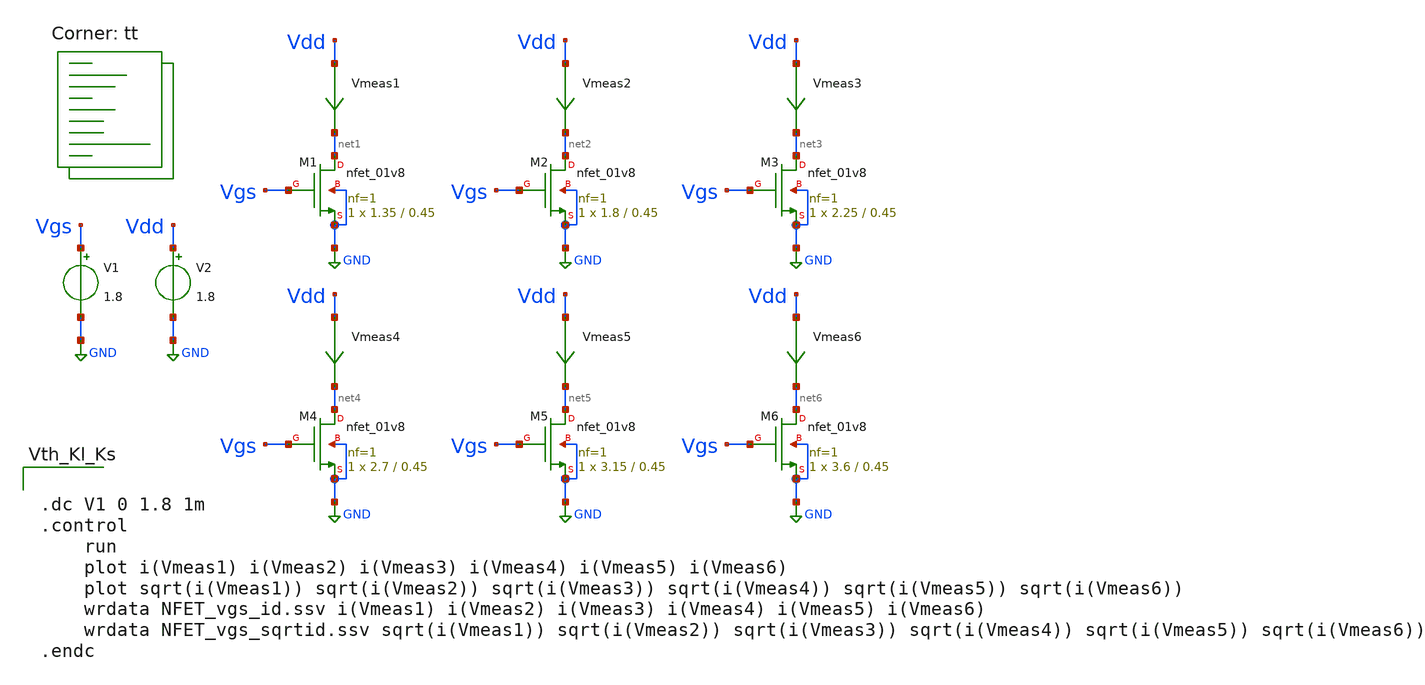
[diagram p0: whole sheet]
** sch_path: opamp_design/Parametros_cmos/NFET_param1.sch
**.subckt NFET_param1
XM1 net1 Vgs GND GND sky130_fd_pr__nfet_01v8 L=0.45 W=1.35 nf=1 ad='int((nf+1)/2) * W/nf * 0.29' as='int((nf+2)/2) * W/nf * 0.29'
+ pd='2*int((nf+1)/2) * (W/nf + 0.29)' ps='2*int((nf+2)/2) * (W/nf + 0.29)' nrd='0.29 / W' nrs='0.29 / W'
+ sa=0 sb=0 sd=0 mult=1 m=1
Vmeas1 Vdd net1 0
.save i(vmeas1)
V2 Vdd GND 1.8
V1 Vgs GND 1.8
XM2 net2 Vgs GND GND sky130_fd_pr__nfet_01v8 L=0.45 W=1.8 nf=1 ad='int((nf+1)/2) * W/nf * 0.29' as='int((nf+2)/2) * W/nf * 0.29'
+ pd='2*int((nf+1)/2) * (W/nf + 0.29)' ps='2*int((nf+2)/2) * (W/nf + 0.29)' nrd='0.29 / W' nrs='0.29 / W'
+ sa=0 sb=0 sd=0 mult=1 m=1
Vmeas2 Vdd net2 0
.save i(vmeas2)
XM3 net3 Vgs GND GND sky130_fd_pr__nfet_01v8 L=0.45 W=2.25 nf=1 ad='int((nf+1)/2) * W/nf * 0.29' as='int((nf+2)/2) * W/nf * 0.29'
+ pd='2*int((nf+1)/2) * (W/nf + 0.29)' ps='2*int((nf+2)/2) * (W/nf + 0.29)' nrd='0.29 / W' nrs='0.29 / W'
+ sa=0 sb=0 sd=0 mult=1 m=1
Vmeas3 Vdd net3 0
.save i(vmeas3)
XM4 net4 Vgs GND GND sky130_fd_pr__nfet_01v8 L=0.45 W=2.7 nf=1 ad='int((nf+1)/2) * W/nf * 0.29' as='int((nf+2)/2) * W/nf * 0.29'
+ pd='2*int((nf+1)/2) * (W/nf + 0.29)' ps='2*int((nf+2)/2) * (W/nf + 0.29)' nrd='0.29 / W' nrs='0.29 / W'
+ sa=0 sb=0 sd=0 mult=1 m=1
Vmeas4 Vdd net4 0
.save i(vmeas4)
XM5 net5 Vgs GND GND sky130_fd_pr__nfet_01v8 L=0.45 W=3.15 nf=1 ad='int((nf+1)/2) * W/nf * 0.29' as='int((nf+2)/2) * W/nf * 0.29'
+ pd='2*int((nf+1)/2) * (W/nf + 0.29)' ps='2*int((nf+2)/2) * (W/nf + 0.29)' nrd='0.29 / W' nrs='0.29 / W'
+ sa=0 sb=0 sd=0 mult=1 m=1
Vmeas5 Vdd net5 0
.save i(vmeas5)
XM6 net6 Vgs GND GND sky130_fd_pr__nfet_01v8 L=0.45 W=3.6 nf=1 ad='int((nf+1)/2) * W/nf * 0.29' as='int((nf+2)/2) * W/nf * 0.29'
+ pd='2*int((nf+1)/2) * (W/nf + 0.29)' ps='2*int((nf+2)/2) * (W/nf + 0.29)' nrd='0.29 / W' nrs='0.29 / W'
+ sa=0 sb=0 sd=0 mult=1 m=1
Vmeas6 Vdd net6 0
.save i(vmeas6)
**** begin user architecture code
.lib $::SKYWATER_MODELS/sky130.lib.spice tt


.dc V1 0 1.8 1m
.control
	run
	plot i(Vmeas1) i(Vmeas2) i(Vmeas3) i(Vmeas4) i(Vmeas5) i(Vmeas6)
	plot sqrt(i(Vmeas1)) sqrt(i(Vmeas2)) sqrt(i(Vmeas3)) sqrt(i(Vmeas4)) sqrt(i(Vmeas5))
+ sqrt(i(Vmeas6))
	wrdata NFET_vgs_id.ssv i(Vmeas1) i(Vmeas2) i(Vmeas3) i(Vmeas4) i(Vmeas5) i(Vmeas6)
	wrdata NFET_vgs_sqrtid.ssv sqrt(i(Vmeas1)) sqrt(i(Vmeas2)) sqrt(i(Vmeas3)) sqrt(i(Vmeas4))
+ sqrt(i(Vmeas5)) sqrt(i(Vmeas6))
.endc


**** end user architecture code
**.ends
.GLOBAL GND
.end
